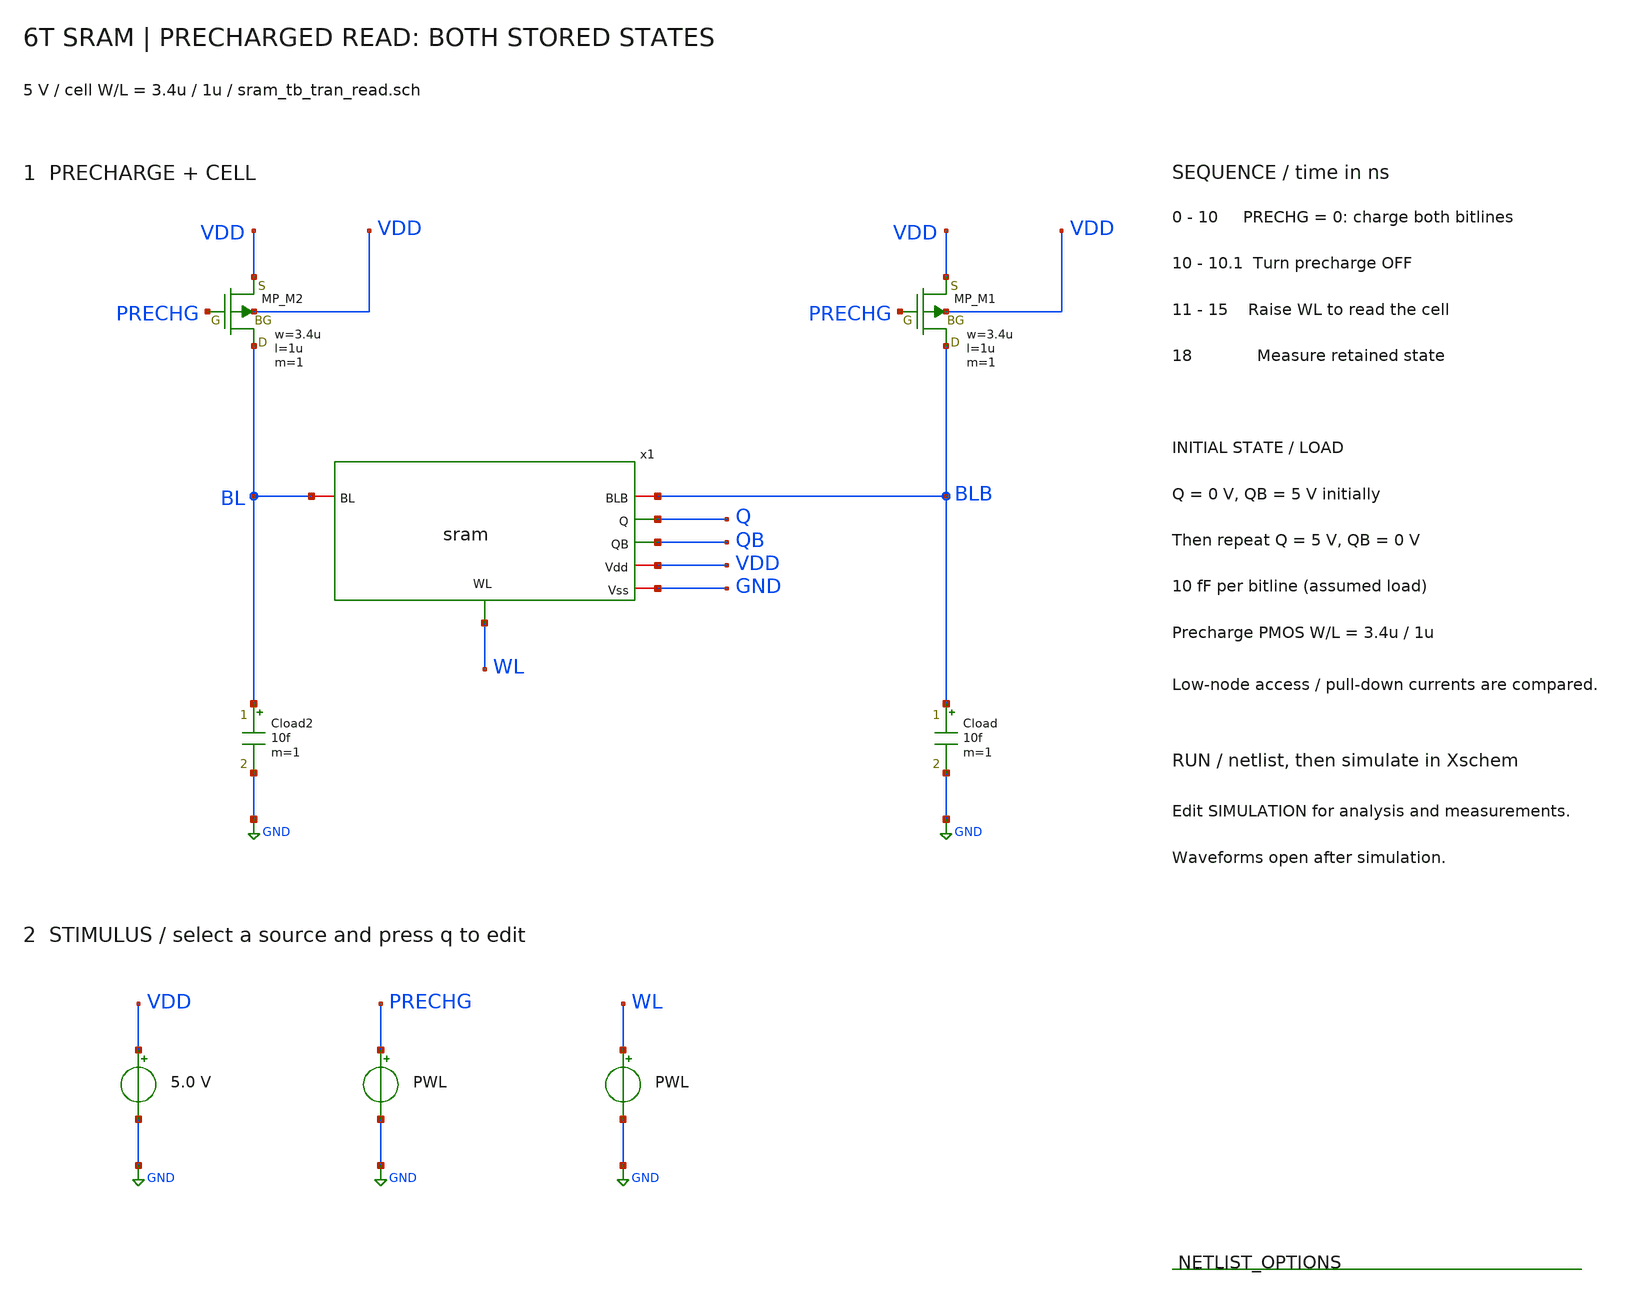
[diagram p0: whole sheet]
** sch_path: member_project/SRAM/PenguinEino/learning/schematics/sram_tb_tran_read.sch
**.subckt sram_tb_tran_read
x1 WL VDD BLB Q QB BL GND sram
XM2 BL PRECHG VDD VDD PMOS w=3.4u l=1u nrd=0 nrs=0 m=1
Cload2 BL GND 10f m=1
XM1 BLB PRECHG VDD VDD PMOS w=3.4u l=1u nrd=0 nrs=0 m=1
Cload BLB GND 10f m=1
Vdd VDD GND 5.0
VPRECHG PRECHG GND PWL(0 0 10n 0 10.1n 5 20n 5)
VWL WL GND PWL(0 0 11n 0 11.1n 5 15n 5 15.1n 0 20n 0)
**** begin user architecture code
 .include $::LIB/ip62_models

.param QINIT=0 QBINIT=5
.ic v(Q)='QINIT' v(QB)='QBINIT'

.control
save all @m.x1.xxm7.m1[id] @m.x1.xxm6.m1[id] @m.x1.xxm1.m1[id] @m.x1.xxm3.m1[id]

tran 0.01n 20n

meas tran BL_read_Q0 find v(BL) at=14n
meas tran BLB_read_Q0 find v(BLB) at=14n
meas tran Q_read_Q0 find v(Q) at=14n
meas tran QB_read_Q0 find v(QB) at=14n
meas tran Q_disturb_Q0 max v(Q) from=11n to=15n
meas tran Q_hold_Q0 find v(Q) at=18n
meas tran QB_hold_Q0 find v(QB) at=18n

let PRECHG_T = V(PRECHG)/5+10
let WL_T = V(WL)/5+8
let BL_T = V(BL)/5+6
let BLB_T = V(BLB)/5+4
let Q_T = V(Q)/5+2
let QB_T = V(QB)/5
let I_Q_ACCESS_uA = @m.x1.xxm7.m1[id]*1e6
let I_QB_ACCESS_uA = @m.x1.xxm6.m1[id]*1e6
let I_Q_ACCESS_MAG_uA = abs(I_Q_ACCESS_uA)
let I_QB_ACCESS_MAG_uA = abs(I_QB_ACCESS_uA)
meas tran I_Q_ACCESS_PEAK_Q0 max I_Q_ACCESS_MAG_uA from=11n to=15n
meas tran I_QB_ACCESS_PEAK_Q0 max I_QB_ACCESS_MAG_uA from=11n to=15n

* Compare currents at the LOW storage node (Q for Q0, QB for Q5).
let I_LOW_ACCESS_uA = abs(@m.x1.xxm7.m1[id])*1e6
let I_LOW_PULLDOWN_uA = abs(@m.x1.xxm1.m1[id])*1e6
meas tran I_LOW_PULLDOWN_PEAK_Q0 max I_LOW_PULLDOWN_uA from=11n to=15n
plot I_LOW_ACCESS_uA I_LOW_PULLDOWN_uA ylabel 'Current magnitude (uA)' title 'READ STRENGTH: Q0, access versus cell pull-down'

plot PRECHG_T WL_T BL_T BLB_T Q_T QB_T ylimit -0.2 11.2 ydelta 1 title 'READ: Q=0, QB=5 V'
plot I_Q_ACCESS_uA I_QB_ACCESS_uA ylabel 'Access current (uA)' title 'READ current: Q=0, QB=5 V'

alterparam QINIT=5
alterparam QBINIT=0
reset
save all @m.x1.xxm7.m1[id] @m.x1.xxm6.m1[id] @m.x1.xxm1.m1[id] @m.x1.xxm3.m1[id]

tran 0.01n 20n

meas tran BL_read_Q5 find v(BL) at=14n
meas tran BLB_read_Q5 find v(BLB) at=14n
meas tran Q_read_Q5 find v(Q) at=14n
meas tran QB_read_Q5 find v(QB) at=14n
meas tran QB_disturb_Q5 max v(QB) from=11n to=15n
meas tran Q_hold_Q5 find v(Q) at=18n
meas tran QB_hold_Q5 find v(QB) at=18n

let PRECHG_T = V(PRECHG)/5+10
let WL_T = V(WL)/5+8
let BL_T = V(BL)/5+6
let BLB_T = V(BLB)/5+4
let Q_T = V(Q)/5+2
let QB_T = V(QB)/5
let I_Q_ACCESS_uA = @m.x1.xxm7.m1[id]*1e6
let I_QB_ACCESS_uA = @m.x1.xxm6.m1[id]*1e6
let I_Q_ACCESS_MAG_uA = abs(I_Q_ACCESS_uA)
let I_QB_ACCESS_MAG_uA = abs(I_QB_ACCESS_uA)
meas tran I_Q_ACCESS_PEAK_Q5 max I_Q_ACCESS_MAG_uA from=11n to=15n
meas tran I_QB_ACCESS_PEAK_Q5 max I_QB_ACCESS_MAG_uA from=11n to=15n

* Compare currents at the LOW storage node (Q for Q0, QB for Q5).
let I_LOW_ACCESS_uA = abs(@m.x1.xxm6.m1[id])*1e6
let I_LOW_PULLDOWN_uA = abs(@m.x1.xxm3.m1[id])*1e6
meas tran I_LOW_PULLDOWN_PEAK_Q5 max I_LOW_PULLDOWN_uA from=11n to=15n
plot I_LOW_ACCESS_uA I_LOW_PULLDOWN_uA ylabel 'Current magnitude (uA)' title 'READ STRENGTH: Q5, access versus cell pull-down'

plot PRECHG_T WL_T BL_T BLB_T Q_T QB_T ylimit -0.2 11.2 ydelta 1 title 'READ: Q=5 V, QB=0'
plot I_Q_ACCESS_uA I_QB_ACCESS_uA ylabel 'Access current (uA)' title 'READ current: Q=5 V, QB=0'

.endc

**** end user architecture code
**.ends
.GLOBAL GND
.end
